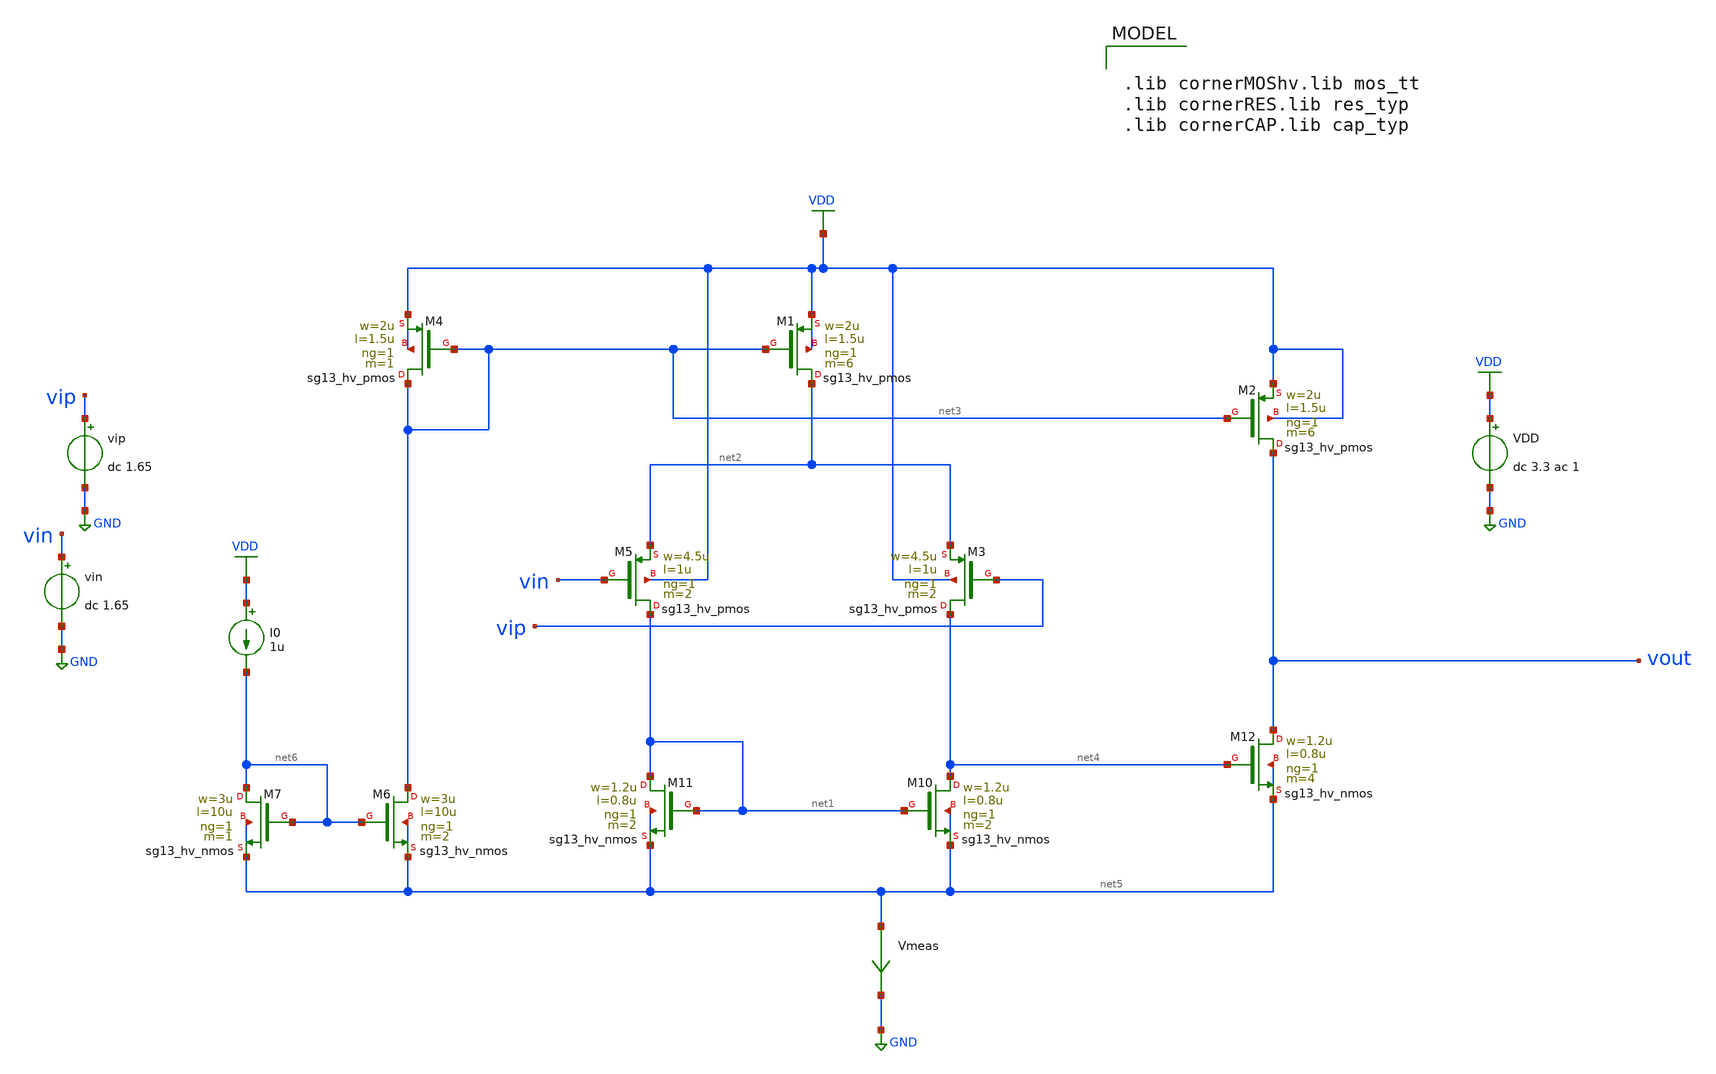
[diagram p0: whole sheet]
** sch_path: dependencies/ClockExtractor/ClockExtractor-main/testbenches/ac/xschem/TowStageOTA_PSRR_2026.sch
**.subckt TowStageOTA_PSRR_2026
vip vip GND dc 1.65
VDD VDD GND dc 3.3 ac 1
XM4 net3 net3 VDD VDD sg13_hv_pmos w=2u l=1.5u ng=1 m=1 mm_ok=1
XM1 net2 net3 VDD VDD sg13_hv_pmos w=2u l=1.5u ng=1 m=6 mm_ok=1
XM2 vout net3 VDD VDD sg13_hv_pmos w=2u l=1.5u ng=1 m=6 mm_ok=1
XM3 net4 vip net2 VDD sg13_hv_pmos w=4.5u l=1u ng=1 m=2 mm_ok=1
XM5 net1 vin net2 VDD sg13_hv_pmos w=4.5u l=1u ng=1 m=2 mm_ok=1
XM10 net4 net1 net5 net5 sg13_hv_nmos w=1.2u l=0.8u ng=1 m=2 mm_ok=1
XM11 net1 net1 net5 net5 sg13_hv_nmos w=1.2u l=0.8u ng=1 m=2 mm_ok=1
XM12 vout net4 net5 net5 sg13_hv_nmos w=1.2u l=0.8u ng=1 m=4 mm_ok=1
I0 VDD net6 1u
Vmeas net5 GND 0
.save i(vmeas)
XM6 net3 net6 net5 net5 sg13_hv_nmos w=3u l=10u ng=1 m=2 mm_ok=1
XM7 net6 net6 net5 net5 sg13_hv_nmos w=3u l=10u ng=1 m=1 mm_ok=1
vin vin GND dc 1.65
**** begin user architecture code


.param temp=27
.control
save all

  op
  ac dec 200 1 100Meg

  let psrr_db = 20*log10(abs(v(vout)/v(VDD)))

  meas ac psrr_dc     FIND psrr_db AT=1
  meas ac psrr_100    FIND psrr_db AT=100
  meas ac psrr_1k     FIND psrr_db AT=1k
  meas ac psrr_10k    FIND psrr_db AT=10k
  meas ac psrr_100k   FIND psrr_db AT=100k
  meas ac psrr_13M56  FIND psrr_db AT=13.56Meg

  print psrr_dc psrr_100 psrr_1k psrr_10k psrr_100k psrr_13M56
  plot psrr_db
write TowStageOTA_PSRR_2026.raw
.endc



.lib cornerMOShv.lib mos_tt
.lib cornerRES.lib res_typ
.lib cornerCAP.lib cap_typ

**** end user architecture code
**.ends
.GLOBAL GND
.GLOBAL VDD
.end
